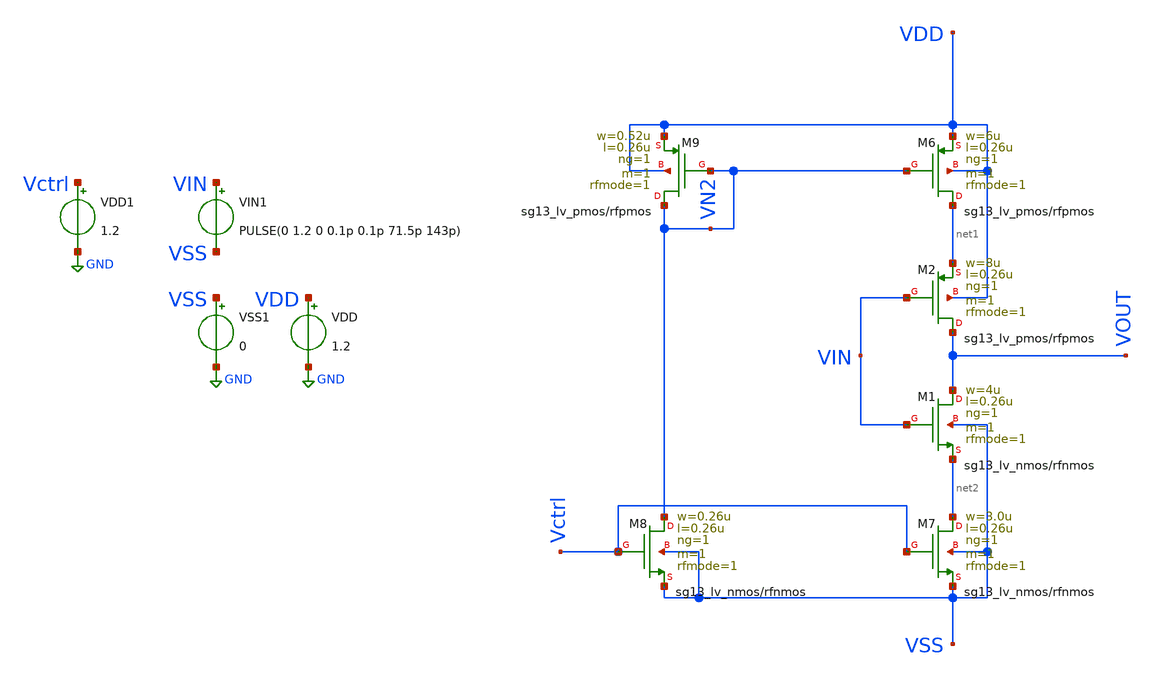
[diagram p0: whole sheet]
** sch_path: inverter.sch
**.subckt inverter
XM9 VN2 VN2 VDD VDD sg13_lv_pmos w=0.52u l=0.26u ng=1 m=1 rfmode=1 mm_ok=1
XM6 net1 VN2 VDD VDD sg13_lv_pmos w=6u l=0.26u ng=1 m=1 rfmode=1 mm_ok=1
XM2 VOUT VIN net1 VDD sg13_lv_pmos w=8u l=0.26u ng=1 m=1 rfmode=1 mm_ok=1
XM8 VN2 Vctrl VSS VSS sg13_lv_nmos w=0.26u l=0.26u ng=1 m=1 rfmode=1 mm_ok=1
XM7 net2 Vctrl VSS VSS sg13_lv_nmos w=3.0u l=0.26u ng=1 m=1 rfmode=1 mm_ok=1
XM1 VOUT VIN net2 VSS sg13_lv_nmos w=4u l=0.26u ng=1 m=1 rfmode=1 mm_ok=1
VDD VDD GND 1.2
VSS1 VSS GND 0
VIN1 VIN VSS PULSE(0 1.2 0 0.1p 0.1p 71.5p 143p)
VDD1 Vctrl GND 1.2
**.ends
.GLOBAL GND
.end
